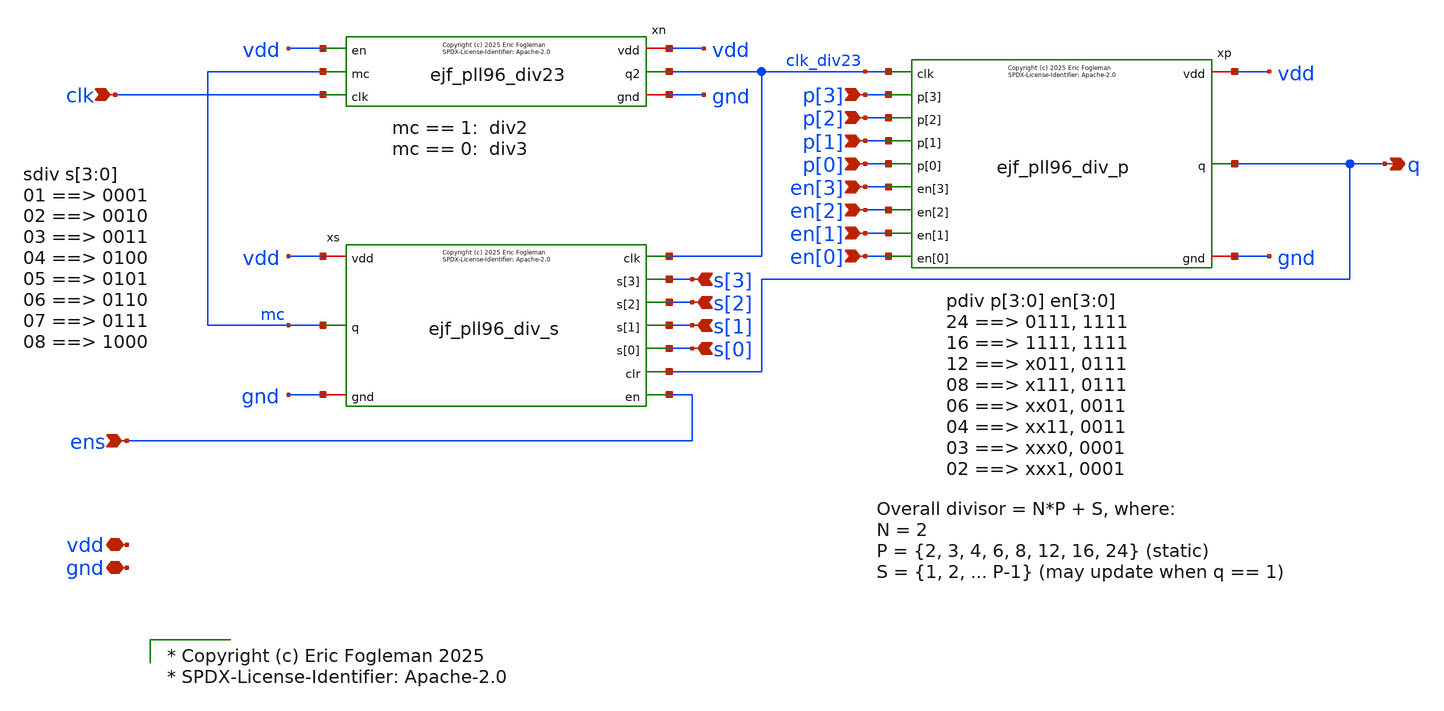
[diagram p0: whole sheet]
** sch_path: xschem/ejf_pll96_div_mm.sch
* xschem/ejf_pll96_div23.sym:
* Copyright (c) 2025 Eric Fogleman

* Copyright (c) Eric Fogleman 2025
* SPDX-License-Identifier: Apache-2.0

**.subckt ejf_pll96_div_mm gnd clk q vdd p[3] p[2] p[1] p[0] en[3] en[2] en[1] s[0] s[1] s[2] s[3]
*+ ens en[0]
*.iopin gnd
*.ipin clk
*.opin q
*.iopin vdd
*.ipin p[3]
*.ipin p[2]
*.ipin p[1]
*.ipin p[0]
*.ipin en[3]
*.ipin en[2]
*.ipin en[1]
*.ipin s[0]
*.ipin s[1]
*.ipin s[2]
*.ipin s[3]
*.ipin ens
*.ipin en[0]
xn clk_div23 clk mc vdd gnd vdd ejf_pll96_div23
xp clk_div23 p[0] en[1] p[1] q en[2] p[2] en[3] p[3] vdd gnd en[0] ejf_pll96_div_p
xs clk_div23 s[0] s[1] s[3] s[2] q mc vdd gnd ens ejf_pll96_div_s
**.ends

* expanding   symbol:  ejf_pll96_div23.sym # of pins=6
** sym_path: xschem/ejf_pll96_div23.sym
** sch_path: xschem/ejf_pll96_div23.sch
.subckt ejf_pll96_div23 q2 clk mc vdd gnd en
*.ipin clk
*.ipin mc
*.opin q2
*.iopin vdd
*.iopin gnd
*.ipin en
x3 q1 mc net1 gnd gnd vdd vdd d2 sky130_fd_sc_ls__o21a_1
x1 clk net1 en gnd gnd vdd vdd q1 sky130_fd_sc_ls__dfstp_2
x2 clk d2 en gnd gnd vdd vdd q2 net1 sky130_fd_sc_ls__dfsbp_2
**** begin user architecture code

* Copyright (c) Eric Fogleman 2025
* SPDX-License-Identifier: Apache-2.0

**** end user architecture code
.ends


* expanding   symbol:  ejf_pll96_div_p.sym # of pins=12
** sym_path: xschem/ejf_pll96_div_p.sym
** sch_path: xschem/ejf_pll96_div_p.sch
.subckt ejf_pll96_div_p clk p[0] en[1] p[1] q en[2] p[2] en[3] p[3] vdd gnd en[0]
*.iopin vdd
*.iopin gnd
*.ipin clk
*.ipin p[1]
*.ipin p[2]
*.ipin p[3]
*.ipin en[3]
*.ipin en[2]
*.opin q
*.ipin en[1]
*.ipin en[0]
*.ipin p[0]
x0 q0 clk p[0] vdd gnd en[0] ejf_pll96_div23
x1 q1 q0 p[1] vdd gnd en[1] ejf_pll96_div23
x2 q2 q1 p[2] vdd gnd en[2] ejf_pll96_div23
x3 q3 q2 p[3] vdd gnd en[3] ejf_pll96_div23
x6 q0 q1 q2 q3 gnd gnd vdd vdd eq0123 sky130_fd_sc_ls__and4_2
x4 clk eq0123 en[0] gnd gnd vdd vdd q sky130_fd_sc_ls__dfrtp_2
**** begin user architecture code

* Copyright (c) Eric Fogleman 2025
* SPDX-License-Identifier: Apache-2.0

**** end user architecture code
.ends


* expanding   symbol:  ejf_pll96_div_s.sym # of pins=10
** sym_path: xschem/ejf_pll96_div_s.sym
** sch_path: xschem/ejf_pll96_div_s.sch
.subckt ejf_pll96_div_s clk s[0] s[1] s[3] s[2] clr q vdd gnd en
*.ipin s[0]
*.ipin s[1]
*.ipin s[2]
*.ipin s[3]
*.ipin clk
*.iopin vdd
*.iopin gnd
*.ipin en
*.ipin clr
*.opin q
x1 q0 s[0] gnd gnd vdd vdd eq0 sky130_fd_sc_ls__xnor2_1
xdff0 clk q0_b q_b gnd gnd vdd vdd q0 q0_b sky130_fd_sc_ls__dfrbp_1
x5 q1 s[1] gnd gnd vdd vdd eq1 sky130_fd_sc_ls__xnor2_1
xdff1 q0_b q1_b q_b gnd gnd vdd vdd q1 q1_b sky130_fd_sc_ls__dfrbp_1
x7 q2 s[2] gnd gnd vdd vdd eq2 sky130_fd_sc_ls__xnor2_1
xdff2 q1_b q2_b q_b gnd gnd vdd vdd q2 q2_b sky130_fd_sc_ls__dfrbp_1
x9 q3 s[3] gnd gnd vdd vdd eq3 sky130_fd_sc_ls__xnor2_1
xdff3 q2_b q3_b q_b gnd gnd vdd vdd q3 q3_b sky130_fd_sc_ls__dfrbp_1
x8 en gnd gnd vdd vdd en_b sky130_fd_sc_ls__inv_1
x4 q eq0123 en_b gnd gnd vdd vdd q_b sky130_fd_sc_ls__nor3_2
x2 eq3 eq2 eq1 eq0 gnd gnd vdd vdd eq0123 sky130_fd_sc_ls__and4_2
x11 en clr q_b gnd gnd vdd vdd q sky130_fd_sc_ls__a21oi_2
**** begin user architecture code

* Copyright (c) Eric Fogleman 2025
* SPDX-License-Identifier: Apache-2.0

**** end user architecture code
.ends

.end
